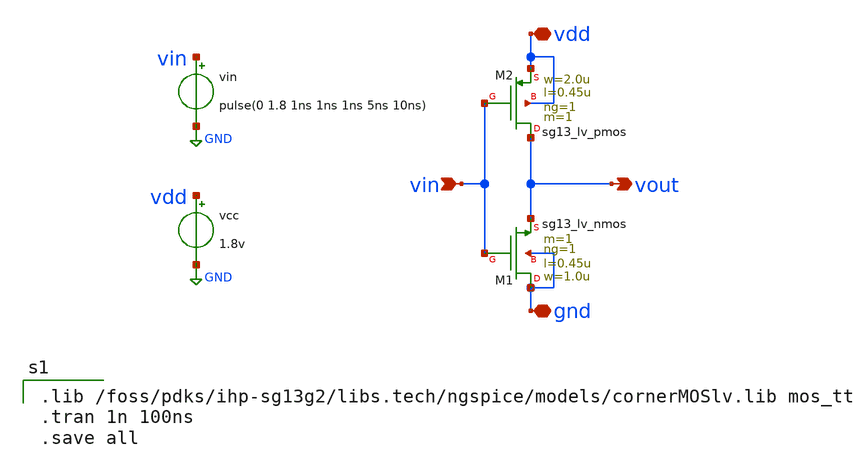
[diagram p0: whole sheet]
** sch_path: content/simulation_files/xschem/07_inverter.sch
* Copyright 2023 IHP PDK Authors
**.subckt 07_inverter vdd gnd vin vout
*.iopin vdd
*.iopin gnd
*.ipin vin
*.opin vout
XM1 gnd vin vout gnd sg13_lv_nmos w=1.0u l=0.45u ng=1 m=1 mm_ok=1
XM2 vout vin vdd vdd sg13_lv_pmos w=2.0u l=0.45u ng=1 m=1 mm_ok=1
vcc vdd GND 1.8v
vin vin GND pulse(0 1.8 1ns 1ns 1ns 5ns 10ns)
**** begin user architecture code

.lib /foss/pdks/ihp-sg13g2/libs.tech/ngspice/models/cornerMOSlv.lib mos_tt
.tran 1n 100ns
.save all

**** end user architecture code
**.ends
.GLOBAL GND
.end
